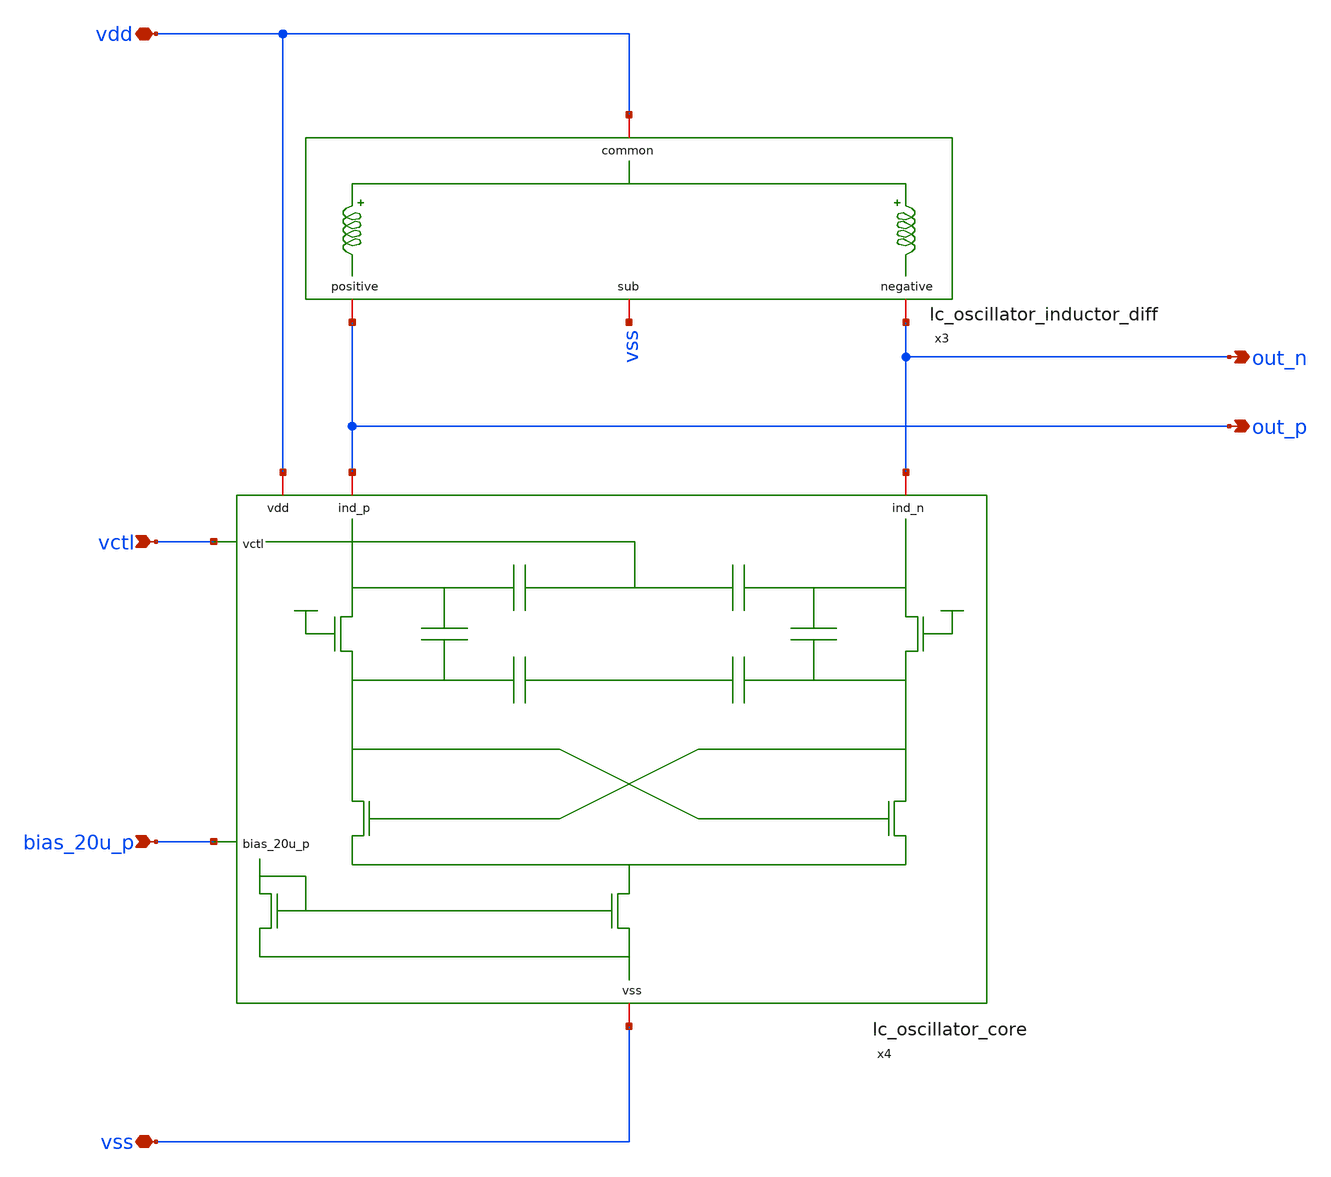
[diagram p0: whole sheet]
** sch_path: design/lc_oscillator/lc_oscillator.sch
**.subckt lc_oscillator vctl vss bias_20u_p vdd out_p out_n
*.ipin vctl
*.iopin vss
*.ipin bias_20u_p
*.iopin vdd
*.opin out_p
*.opin out_n
x3 vdd out_p out_n vss lc_oscillator_inductor_diff
x4 vdd out_p vctl out_n bias_20u_p vss lc_oscillator_core
**.ends

* expanding   symbol:  lc_oscillator_inductor_diff/lc_oscillator_inductor_diff.sym # of pins=4
** sym_path: design/lc_oscillator_inductor_diff/lc_oscillator_inductor_diff.sym
** sch_path: design/lc_oscillator_inductor_diff/lc_oscillator_inductor_diff.sch
.subckt lc_oscillator_inductor_diff common positive negative sub
*.iopin common
*.iopin positive
*.iopin sub
*.iopin negative
xlneg common negative sub lc_oscillator_inductor
xlpos common positive sub lc_oscillator_inductor
.ends


* expanding   symbol:  lc_oscillator_core/lc_oscillator_core.sym # of pins=6
** sym_path: design/lc_oscillator_core/lc_oscillator_core.sym
** sch_path: design/lc_oscillator_core/lc_oscillator_core.sch
.subckt lc_oscillator_core vdd ind_p vctl ind_n bias_20u_p vss
*.ipin vctl
*.iopin vss
*.ipin bias_20u_p
*.iopin vdd
*.iopin ind_n
*.iopin ind_p
XM2 bias_20u_p bias_20u_p vss vss sky130_fd_pr__nfet_01v8_lvt L=0.5 W=5 nf=1 ad='int((nf+1)/2) * W/nf * 0.29'
+ as='int((nf+2)/2) * W/nf * 0.29' pd='2*int((nf+1)/2) * (W/nf + 0.29)' ps='2*int((nf+2)/2) * (W/nf + 0.29)'
+ nrd='0.29 / W' nrs='0.29 / W' sa=0 sb=0 sd=0 mult=2 m=2
XM1 net3 bias_20u_p vss vss sky130_fd_pr__nfet_01v8_lvt L=0.5 W=5 nf=1 ad='int((nf+1)/2) * W/nf * 0.29'
+ as='int((nf+2)/2) * W/nf * 0.29' pd='2*int((nf+1)/2) * (W/nf + 0.29)' ps='2*int((nf+2)/2) * (W/nf + 0.29)'
+ nrd='0.29 / W' nrs='0.29 / W' sa=0 sb=0 sd=0 mult=32 m=32
XM3 net3 bias_20u_p vss vss sky130_fd_pr__nfet_01v8_lvt L=0.5 W=5 nf=1 ad='int((nf+1)/2) * W/nf * 0.29'
+ as='int((nf+2)/2) * W/nf * 0.29' pd='2*int((nf+1)/2) * (W/nf + 0.29)' ps='2*int((nf+2)/2) * (W/nf + 0.29)'
+ nrd='0.29 / W' nrs='0.29 / W' sa=0 sb=0 sd=0 mult=32 m=32
XC1 ind_p net2 sky130_fd_pr__cap_mim_m3_1 W=6 L=6 MF=4 m=4
XC2 ind_n net1 sky130_fd_pr__cap_mim_m3_1 W=6 L=6 MF=4 m=4
XC3 net2 net4 sky130_fd_pr__cap_mim_m3_1 W=6 L=6 MF=1 m=1
XC4 net1 net4 sky130_fd_pr__cap_mim_m3_1 W=6 L=6 MF=1 m=1
XM4 ind_p vdd net2 vss sky130_fd_pr__nfet_01v8_lvt L=0.15 W=40 nf=8 ad='int((nf+1)/2) * W/nf * 0.29'
+ as='int((nf+2)/2) * W/nf * 0.29' pd='2*int((nf+1)/2) * (W/nf + 0.29)' ps='2*int((nf+2)/2) * (W/nf + 0.29)'
+ nrd='0.29 / W' nrs='0.29 / W' sa=0 sb=0 sd=0 mult=1 m=1
XM5 ind_n vdd net1 vss sky130_fd_pr__nfet_01v8_lvt L=0.15 W=40 nf=8 ad='int((nf+1)/2) * W/nf * 0.29'
+ as='int((nf+2)/2) * W/nf * 0.29' pd='2*int((nf+1)/2) * (W/nf + 0.29)' ps='2*int((nf+2)/2) * (W/nf + 0.29)'
+ nrd='0.29 / W' nrs='0.29 / W' sa=0 sb=0 sd=0 mult=1 m=1
XM6 net2 net1 net3 vss sky130_fd_pr__nfet_01v8_lvt L=0.15 W=40 nf=8 ad='int((nf+1)/2) * W/nf * 0.29'
+ as='int((nf+2)/2) * W/nf * 0.29' pd='2*int((nf+1)/2) * (W/nf + 0.29)' ps='2*int((nf+2)/2) * (W/nf + 0.29)'
+ nrd='0.29 / W' nrs='0.29 / W' sa=0 sb=0 sd=0 mult=1 m=1
XM7 net1 net2 net3 vss sky130_fd_pr__nfet_01v8_lvt L=0.15 W=40 nf=8 ad='int((nf+1)/2) * W/nf * 0.29'
+ as='int((nf+2)/2) * W/nf * 0.29' pd='2*int((nf+1)/2) * (W/nf + 0.29)' ps='2*int((nf+2)/2) * (W/nf + 0.29)'
+ nrd='0.29 / W' nrs='0.29 / W' sa=0 sb=0 sd=0 mult=1 m=1
x1 vctl ind_p lc_oscillator_varactor
x2 vctl ind_n lc_oscillator_varactor
.ends


* expanding   symbol:  lc_oscillator_inductor/lc_oscillator_inductor.sym # of pins=3
** sym_path: design/lc_oscillator_inductor/lc_oscillator_inductor.sym
** sch_path: design/lc_oscillator_inductor/lc_oscillator_inductor.sch
.subckt lc_oscillator_inductor p1 p2 sub
*.iopin p2
*.iopin p1
*.iopin sub
L1 net1 p1 1.028n m=1
C1 p1 net2 62.02f m=1
R1 net2 sub 16.03 m=1
C2 p1 p2 0.1f m=1
C3 p2 net3 62.31f m=1
R2 net3 sub 15.88 m=1
R3 p2 net1 3.6825 m=1
.ends


* expanding   symbol:  lc_oscillator_varactor/lc_oscillator_varactor.sym # of pins=2
** sym_path: design/lc_oscillator_varactor/lc_oscillator_varactor.sym
** sch_path: design/lc_oscillator_varactor/lc_oscillator_varactor.sch
.subckt lc_oscillator_varactor p m
*.iopin p
*.iopin m
XM1 p m p p sky130_fd_pr__pfet_01v8 L=4 W=4 nf=1 ad='int((nf+1)/2) * W/nf * 0.29' as='int((nf+2)/2) * W/nf * 0.29'
+ pd='2*int((nf+1)/2) * (W/nf + 0.29)' ps='2*int((nf+2)/2) * (W/nf + 0.29)' nrd='0.29 / W' nrs='0.29 / W'
+ sa=0 sb=0 sd=0 mult=1 m=1
.ends

.end
